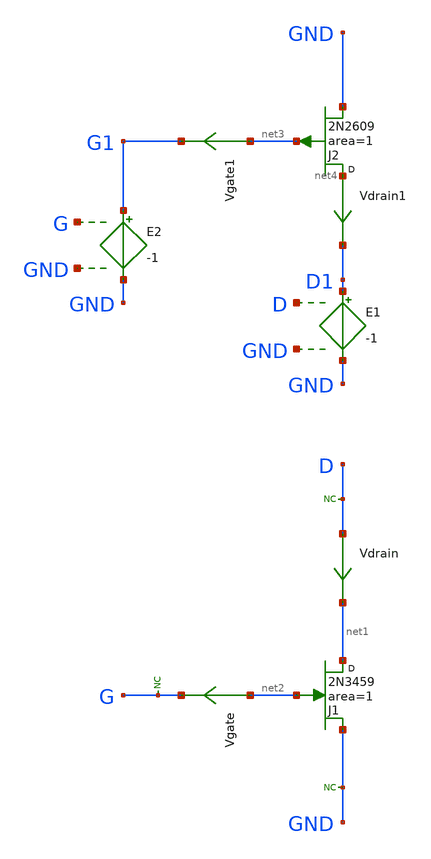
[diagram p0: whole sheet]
** sch_path: sky130A/xschem_libs/sky130_tests_ase/test_jfet/schematic/test_jfet.sch
**.subckt test_jfet
J1 net1 net2 GND 2N3459 area=1 m=1
* noconn GND
* noconn D
* noconn G
Vgate net2 G 0
.save i(vgate)
Vdrain D net1 0
.save i(vdrain)
J2 net4 net3 GND 2N2609 area=1 m=1
Vgate1 net3 G1 0
.save i(vgate1)
Vdrain1 net4 D1 0
.save i(vdrain1)
E1 D1 GND D GND -1
E2 G1 GND G GND -1
**.ends
.end
